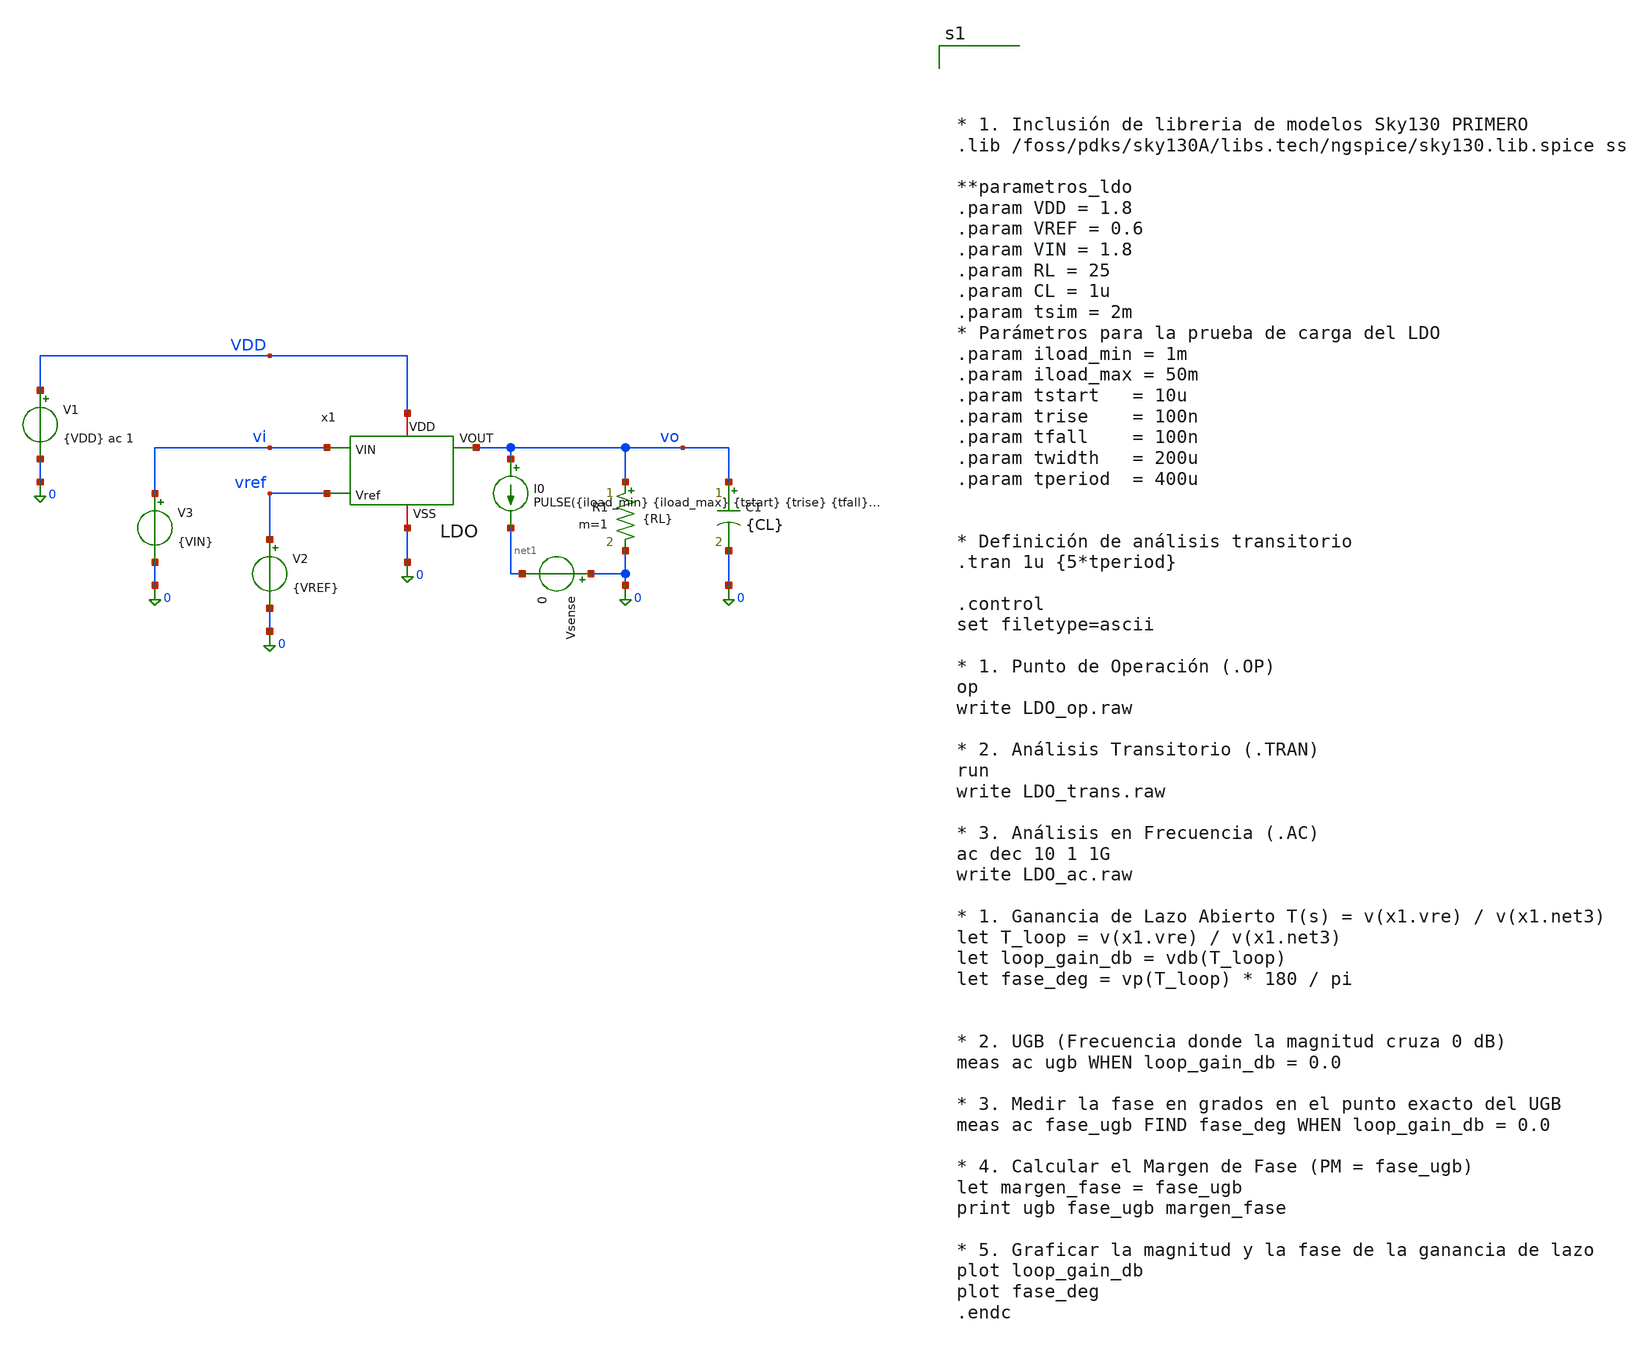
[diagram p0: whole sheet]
** sch_path: xschem/ldo_tb.sch
**.subckt ldo_tb
x1 vi vo VDD vref 0 LDO
V1 VDD 0 {VDD} ac 1
V2 vref 0 {VREF}
V3 vi 0 {VIN}
R1 vo 0 {RL} m=1
C1 vo 0 {CL} m=1
I0 vo net1 PULSE({iload_min} {iload_max} {tstart} {trise} {tfall} {twidth} {tperiod})
Vsense 0 net1 0
**** begin user architecture code




* 1. Inclusión de libreria de modelos Sky130 PRIMERO
.lib /foss/pdks/sky130A/libs.tech/ngspice/sky130.lib.spice ss

**parametros_ldo
.param VDD = 1.8
.param VREF = 0.6
.param VIN = 1.8
.param RL = 25
.param CL = 1u
.param tsim = 2m
* Parámetros para la prueba de carga del LDO
.param iload_min = 1m
.param iload_max = 50m
.param tstart   = 10u
.param trise    = 100n
.param tfall    = 100n
.param twidth   = 200u
.param tperiod  = 400u


* Definición de análisis transitorio
.tran 1u {5*tperiod}

.control
set filetype=ascii

* 1. Punto de Operación (.OP)
op
write LDO_op.raw

* 2. Análisis Transitorio (.TRAN)
run
write LDO_trans.raw

* 3. Análisis en Frecuencia (.AC)
ac dec 10 1 1G
write LDO_ac.raw

* 1. Ganancia de Lazo Abierto T(s) = v(x1.vre) / v(x1.net3)
let T_loop = v(x1.vre) / v(x1.net3)
let loop_gain_db = vdb(T_loop)
let fase_deg = vp(T_loop) * 180 / pi


* 2. UGB (Frecuencia donde la magnitud cruza 0 dB)
meas ac ugb WHEN loop_gain_db = 0.0

* 3. Medir la fase en grados en el punto exacto del UGB
meas ac fase_ugb FIND fase_deg WHEN loop_gain_db = 0.0

* 4. Calcular el Margen de Fase (PM = fase_ugb)
let margen_fase = fase_ugb
print ugb fase_ugb margen_fase

* 5. Graficar la magnitud y la fase de la ganancia de lazo
plot loop_gain_db
plot fase_deg
.endc



**** end user architecture code
**.ends

* expanding   symbol:  /foss/designs/LDO-sky130/xschem/LDO.sym # of pins=5
** sym_path: xschem/LDO.sym
** sch_path: xschem/LDO.sch
.subckt LDO VIN VOUT VDD Vref VSS
*.ipin VIN
*.iopin VDD
*.opin VOUT
*.ipin Vref
*.iopin VSS
x1 VDD net2 Vref net3 net1 VSS OTA
I0 VDD net1 10u
XM1 VOUT net2 VIN VDD sky130_fd_pr__pfet_01v8_lvt L=0.35 W=1000 nf=50 ad='int((50 + 1)/2) * 1000 / 50 * 0.29'
+ as='int((50 + 2)/2) * 1000 / 50 * 0.29' pd='2*int((50 + 1)/2) * (1000 / 50 + 0.29)' ps='2*int((50 + 2)/2) * (1000 / 50 + 0.29)'
+ nrd='0.29 / 1000 ' nrs='0.29 / 1000 ' sa=0 sb=0 sd=0 mult=5 m=5
XR1 Vre VOUT VDD sky130_fd_pr__res_iso_pw W=0.35 L=10 m=1
XR2 VSS Vre VDD sky130_fd_pr__res_iso_pw W=0.35 L=10 m=1
V1 net3 Vre 0 ac 1
XC1 VOUT Vre sky130_fd_pr__cap_mim_m3_2 W=19.5 L=19.5 MF=1 m=1
.ends


* expanding   symbol:  /foss/designs/LDO-sky130/xschem/OTA.sym # of pins=6
** sym_path: xschem/OTA.sym
** sch_path: xschem/OTA.sch
.subckt OTA VDD VO_ota VIN_ota VIP_ota Iref VSS
*.ipin VIN_ota
*.opin VO_ota
*.iopin Iref
*.iopin VSS
*.iopin VDD
*.ipin VIP_ota
XMr Iref Iref VSS VSS sky130_fd_pr__nfet_01v8 L=0.5 W=0.5 nf=1 ad='int((1 + 1)/2) * 0.5 / 1 * 0.29' as='int((1 + 2)/2) * 0.5 / 1 * 0.29'
+ pd='2*int((1 + 1)/2) * (0.5 / 1 + 0.29)' ps='2*int((1 + 2)/2) * (0.5 / 1 + 0.29)' nrd='0.29 / 0.5 ' nrs='0.29 / 0.5 '
+ sa=0 sb=0 sd=0 mult=1 m=1
XMo VO_ota VO_ota1 VDD VDD sky130_fd_pr__pfet_01v8 L=0.5 W=20 nf=1 ad='int((1 + 1)/2) * 20 / 1 * 0.29'
+ as='int((1 + 2)/2) * 20 / 1 * 0.29' pd='2*int((1 + 1)/2) * (20 / 1 + 0.29)' ps='2*int((1 + 2)/2) * (20 / 1 + 0.29)'
+ nrd='0.29 / 20 ' nrs='0.29 / 20 ' sa=0 sb=0 sd=0 mult=1 m=1
XMrc1 Vtail Iref VSS VSS sky130_fd_pr__nfet_01v8 L=0.5 W=2 nf=1 ad='int((1 + 1)/2) * 2 / 1 * 0.29' as='int((1 + 2)/2) * 2 / 1 * 0.29'
+ pd='2*int((1 + 1)/2) * (2 / 1 + 0.29)' ps='2*int((1 + 2)/2) * (2 / 1 + 0.29)' nrd='0.29 / 2 ' nrs='0.29 / 2 '
+ sa=0 sb=0 sd=0 mult=1 m=1
XMc2 VO_ota Iref VSS VSS sky130_fd_pr__nfet_01v8 L=0.5 W=1 nf=1 ad='int((1 + 1)/2) * 1 / 1 * 0.29' as='int((1 + 2)/2) * 1 / 1 * 0.29'
+ pd='2*int((1 + 1)/2) * (1 / 1 + 0.29)' ps='2*int((1 + 2)/2) * (1 / 1 + 0.29)' nrd='0.29 / 1 ' nrs='0.29 / 1 '
+ sa=0 sb=0 sd=0 mult=1 m=1
XMn VGP VIN_ota Vtail VSS sky130_fd_pr__nfet_01v8 L=0.5 W=40 nf=1 ad='int((1 + 1)/2) * 40 / 1 * 0.29'
+ as='int((1 + 2)/2) * 40 / 1 * 0.29' pd='2*int((1 + 1)/2) * (40 / 1 + 0.29)' ps='2*int((1 + 2)/2) * (40 / 1 + 0.29)'
+ nrd='0.29 / 40 ' nrs='0.29 / 40 ' sa=0 sb=0 sd=0 mult=1 m=1
XMp VO_ota1 VIP_ota Vtail VSS sky130_fd_pr__nfet_01v8 L=0.5 W=40 nf=1 ad='int((1 + 1)/2) * 40 / 1 * 0.29'
+ as='int((1 + 2)/2) * 40 / 1 * 0.29' pd='2*int((1 + 1)/2) * (40 / 1 + 0.29)' ps='2*int((1 + 2)/2) * (40 / 1 + 0.29)'
+ nrd='0.29 / 40 ' nrs='0.29 / 40 ' sa=0 sb=0 sd=0 mult=1 m=1
XMpr VO_ota1 VGP VDD VDD sky130_fd_pr__pfet_01v8 L=0.5 W=40 nf=1 ad='int((1 + 1)/2) * 40 / 1 * 0.29'
+ as='int((1 + 2)/2) * 40 / 1 * 0.29' pd='2*int((1 + 1)/2) * (40 / 1 + 0.29)' ps='2*int((1 + 2)/2) * (40 / 1 + 0.29)'
+ nrd='0.29 / 40 ' nrs='0.29 / 40 ' sa=0 sb=0 sd=0 mult=1 m=1
XMnr VGP VGP VDD VDD sky130_fd_pr__pfet_01v8 L=0.5 W=40 nf=1 ad='int((1 + 1)/2) * 40 / 1 * 0.29' as='int((1 + 2)/2) * 40 / 1 * 0.29'
+ pd='2*int((1 + 1)/2) * (40 / 1 + 0.29)' ps='2*int((1 + 2)/2) * (40 / 1 + 0.29)' nrd='0.29 / 40 ' nrs='0.29 / 40 '
+ sa=0 sb=0 sd=0 mult=1 m=1
XR1 VO_ota1 net1 VDD sky130_fd_pr__res_high_po W=0.35 L=360 mult=1 m=1
XC1 VO_ota net1 sky130_fd_pr__cap_mim_m3_2 W=50 L=50 MF=1 m=1
.ends

.end
